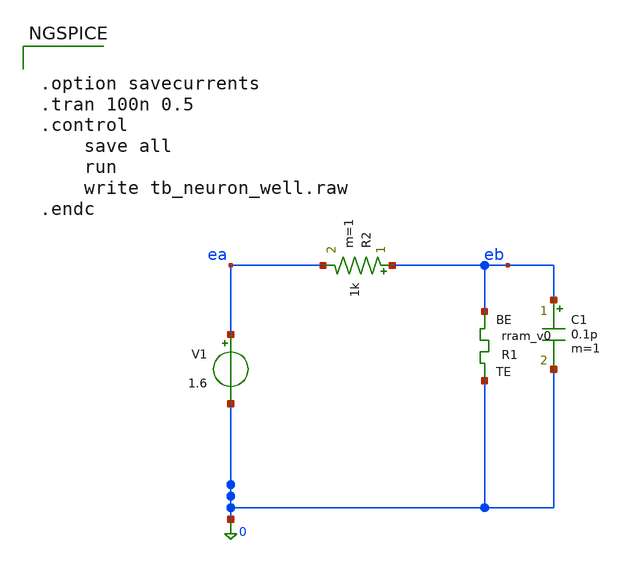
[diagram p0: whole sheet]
** sch_path: memristor_models/wellposed/tb_neuron_well.sch
**.subckt tb_neuron_well
V1 ea 0 1.6
XR1 0 eb rram_v0
C1 eb 0 0.1p m=1
R2 eb ea 1k m=1
**** begin user architecture code

** opencircuitdesign pdks install
.inc $::SKYWATER_MODELS/rram_v0.spice



.option savecurrents
.tran 100n 0.5
.control
	save all
	run
	write tb_neuron_well.raw
.endc



**** end user architecture code
**.ends
.end
